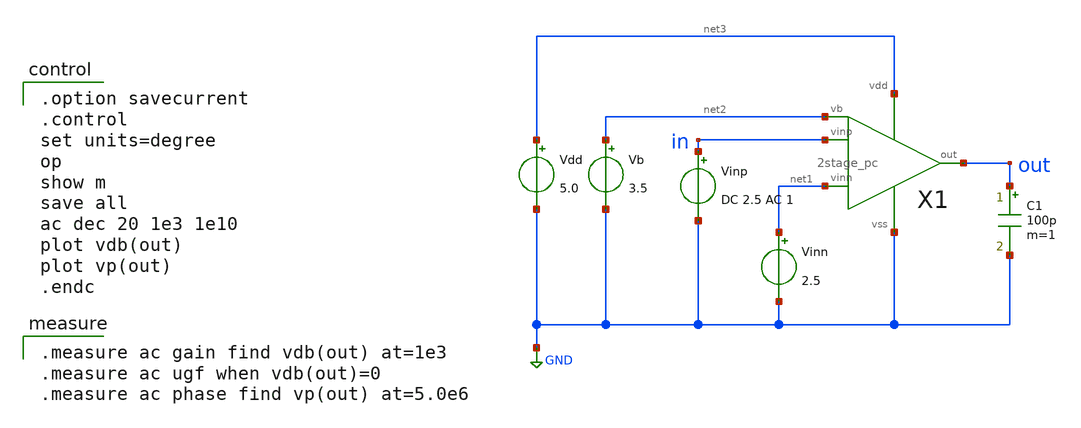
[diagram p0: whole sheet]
** sch_path: OpenSUSI-TR10/opamp/2stage_pc_ac.sch
**.subckt 2stage_pc_ac
Vdd net3 GND 5.0
Vb net2 GND 3.5
Vinn net1 GND 2.5
Vinp in GND DC 2.5 AC 1
C1 out GND 100p m=1
X1 in net1 net2 out net3 GND 2stage_pc
**** begin user architecture code

.option savecurrent
.control
set units=degree
op
show m
save all
ac dec 20 1e3 1e10
plot vdb(out)
plot vp(out)
.endc


.measure ac gain find vdb(out) at=1e3
.measure ac ugf when vdb(out)=0
.measure ac phase find vp(out) at=5.0e6

 .include $::LIB/ip62_models
**** end user architecture code
**.ends

* expanding   symbol:  2stage_pc.sym # of pins=6
** sym_path: 2stage_pc.sym
** sch_path: 2stage_pc.sch
.subckt 2stage_pc vinp vinn vb out vdd vss
*.ipin vinp
*.ipin vinn
*.ipin vb
*.opin out
*.iopin vdd
*.iopin vss
X1 vinp vinn net2 vdd vss vb diff
X2 net2 vb out vdd vss cs
XM6 net1 vb vdd vdd PMOS w=30u l=1u as=0 ad=0 ps=0 pd=0 nrd=0 nrs=0 m=1
XM1 net1 net1 net4 vss NMOS w=10u l=1u as=0 ad=0 ps=0 pd=0 nrd=0 nrs=0 m=1
XM7 net4 net4 vss vss NMOS w=10u l=1u as=0 ad=0 ps=0 pd=0 nrd=0 nrs=0 m=1
XM2 net3 net1 net2 vss NMOS w=20u l=1u as=0 ad=0 ps=0 pd=0 nrd=0 nrs=0 m=1
XC1 net3 out vss F_CSIO c=8.856p x=120u y=120u m=1
.ends


* expanding   symbol:  diff.sym # of pins=6
** sym_path: diff.sym
** sch_path: diff.sch
.subckt diff vinp vinn out vdd vss vb
*.ipin vinn
*.ipin vinp
*.ipin vb
*.opin out
*.iopin vdd
*.iopin vss
M5 net2 vb vdd vdd pmos L=2u W=40u m=1
M1 net1 vinn net2 net2 pmos L=2u W=200u m=1
M2 out vinp net2 net2 pmos L=2u W=200u m=1
M3 net1 net1 vss vss nmos L=2u W=10u m=1
M4 out net1 vss vss nmos L=2u W=10u m=1
.ends


* expanding   symbol:  cs.sym # of pins=5
** sym_path: cs.sym
** sch_path: cs.sch
.subckt cs vin vb out vdd vss
*.ipin vb
*.ipin vin
*.opin out
*.iopin vss
*.iopin vdd
XM6 out vb vdd vdd PMOS w=270u l=1u as=0 ad=0 ps=0 pd=0 nrd=0 nrs=0 m=1
XM7 out vin vss vss NMOS w=90u l=1u as=0 ad=0 ps=0 pd=0 nrd=0 nrs=0 m=1
.ends

.GLOBAL GND
.end
